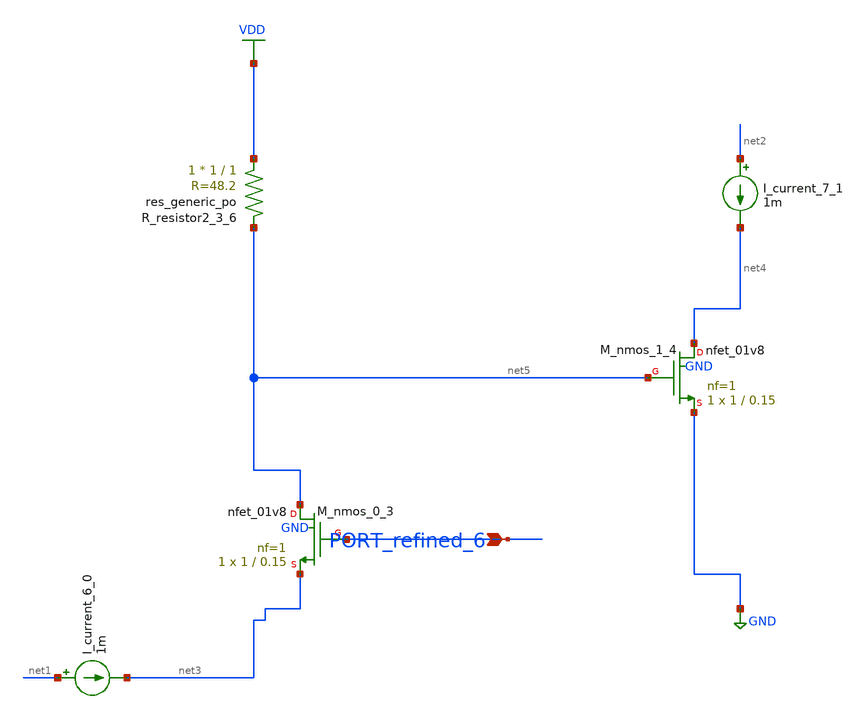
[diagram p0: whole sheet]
** sch_path: schematics/AMSNet/550.sch
**.subckt 550 PORT_refined_6
*.ipin PORT_refined_6
I_current_6_0 net1 net3 1m
I_current_7_1 net2 net4 1m
XM_nmos_0_3 net5 PORT_refined_6 net3 GND sky130_fd_pr__nfet_01v8 L=0.15 W=1 nf=1 ad='int((1 + 1)/2) * 1 / 1 * 0.29'
+ as='int((1 + 2)/2) * 1 / 1 * 0.29' pd='2*int((1 + 1)/2) * (1 / 1 + 0.29)' ps='2*int((1 + 2)/2) * (1 / 1 + 0.29)'
+ nrd='0.29 / 1 ' nrs='0.29 / 1 ' sa=0 sb=0 sd=0 mult=1 m=1
XM_nmos_1_4 net4 net5 GND GND sky130_fd_pr__nfet_01v8 L=0.15 W=1 nf=1 ad='int((1 + 1)/2) * 1 / 1 * 0.29'
+ as='int((1 + 2)/2) * 1 / 1 * 0.29' pd='2*int((1 + 1)/2) * (1 / 1 + 0.29)' ps='2*int((1 + 2)/2) * (1 / 1 + 0.29)'
+ nrd='0.29 / 1 ' nrs='0.29 / 1 ' sa=0 sb=0 sd=0 mult=1 m=1
XR_resistor2_3_6 VDD net5 sky130_fd_pr__res_generic_po W=1 L=1 m=1
**.ends
.GLOBAL GND
.GLOBAL VDD
.end
